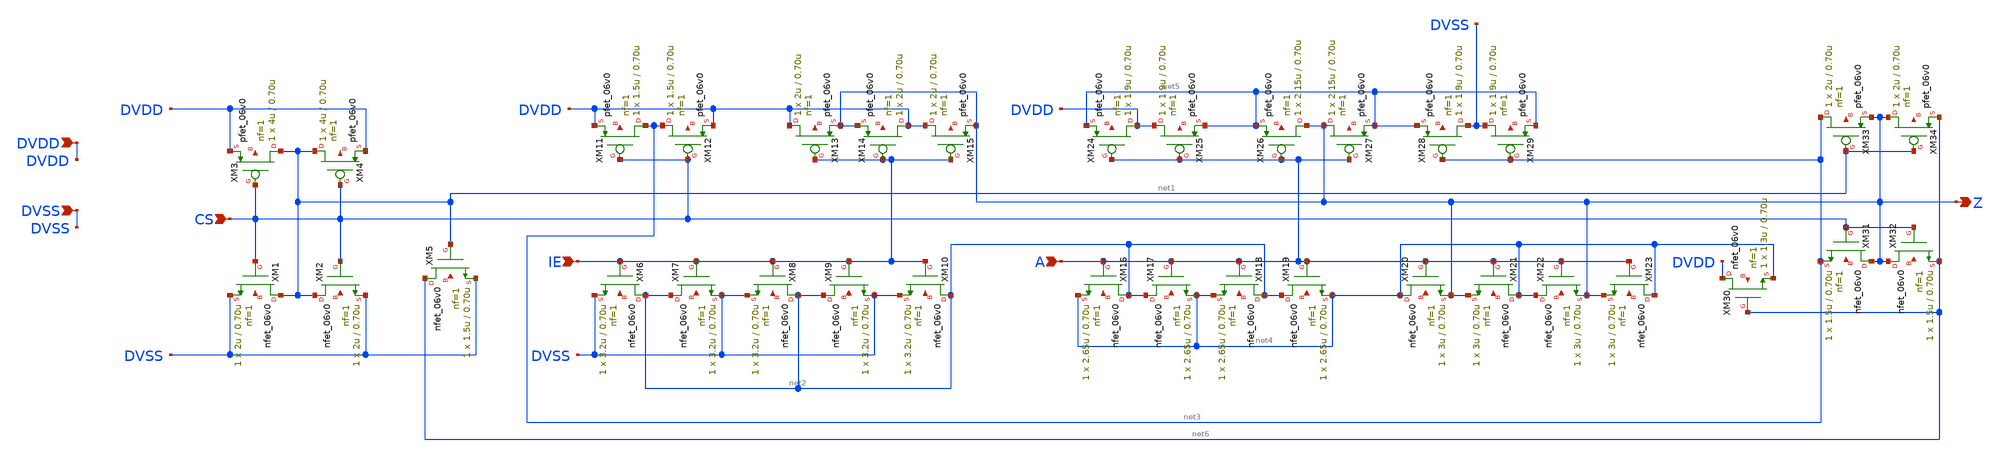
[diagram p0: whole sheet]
** sch_path: gf180mcu_fd_io__bi_24t/comp018green_in_cms_smt.sch
**.subckt comp018green_in_cms_smt CS IE Z A DVDD DVSS
*.ipin CS
*.ipin IE
*.opin Z
*.ipin A
*.ipin DVDD
*.ipin DVSS
XM1 net1 CS DVSS net7 nfet_06v0 L=0.70u W=2u nf=1 ad='int((nf+1)/2) * W/nf * 0.18u' as='int((nf+2)/2) * W/nf * 0.18u'
+ pd='2*int((nf+1)/2) * (W/nf + 0.18u)' ps='2*int((nf+2)/2) * (W/nf + 0.18u)' nrd='0.18u / W' nrs='0.18u / W'
+ sa=0 sb=0 sd=0 m=1
XM2 net1 CS DVSS net8 nfet_06v0 L=0.70u W=2u nf=1 ad='int((nf+1)/2) * W/nf * 0.18u' as='int((nf+2)/2) * W/nf * 0.18u'
+ pd='2*int((nf+1)/2) * (W/nf + 0.18u)' ps='2*int((nf+2)/2) * (W/nf + 0.18u)' nrd='0.18u / W' nrs='0.18u / W'
+ sa=0 sb=0 sd=0 m=1
XM3 net1 CS DVDD net9 pfet_06v0 L=0.70u W=4u nf=1 ad='int((nf+1)/2) * W/nf * 0.18u' as='int((nf+2)/2) * W/nf * 0.18u'
+ pd='2*int((nf+1)/2) * (W/nf + 0.18u)' ps='2*int((nf+2)/2) * (W/nf + 0.18u)' nrd='0.18u / W' nrs='0.18u / W'
+ sa=0 sb=0 sd=0 m=1
XM4 net1 CS DVDD net10 pfet_06v0 L=0.70u W=4u nf=1 ad='int((nf+1)/2) * W/nf * 0.18u' as='int((nf+2)/2) * W/nf * 0.18u'
+ pd='2*int((nf+1)/2) * (W/nf + 0.18u)' ps='2*int((nf+2)/2) * (W/nf + 0.18u)' nrd='0.18u / W' nrs='0.18u / W'
+ sa=0 sb=0 sd=0 m=1
XM5 net6 net1 DVSS net11 nfet_06v0 L=0.70u W=1.5u nf=1 ad='int((nf+1)/2) * W/nf * 0.18u' as='int((nf+2)/2) * W/nf * 0.18u'
+ pd='2*int((nf+1)/2) * (W/nf + 0.18u)' ps='2*int((nf+2)/2) * (W/nf + 0.18u)' nrd='0.18u / W' nrs='0.18u / W'
+ sa=0 sb=0 sd=0 m=1
XM6 net2 IE DVSS net12 nfet_06v0 L=0.70u W=3.2u nf=1 ad='int((nf+1)/2) * W/nf * 0.18u' as='int((nf+2)/2) * W/nf * 0.18u'
+ pd='2*int((nf+1)/2) * (W/nf + 0.18u)' ps='2*int((nf+2)/2) * (W/nf + 0.18u)' nrd='0.18u / W' nrs='0.18u / W'
+ sa=0 sb=0 sd=0 m=1
XM7 net2 IE DVSS net13 nfet_06v0 L=0.70u W=3.2u nf=1 ad='int((nf+1)/2) * W/nf * 0.18u' as='int((nf+2)/2) * W/nf * 0.18u'
+ pd='2*int((nf+1)/2) * (W/nf + 0.18u)' ps='2*int((nf+2)/2) * (W/nf + 0.18u)' nrd='0.18u / W' nrs='0.18u / W'
+ sa=0 sb=0 sd=0 m=1
XM8 net2 IE DVSS net14 nfet_06v0 L=0.70u W=3.2u nf=1 ad='int((nf+1)/2) * W/nf * 0.18u' as='int((nf+2)/2) * W/nf * 0.18u'
+ pd='2*int((nf+1)/2) * (W/nf + 0.18u)' ps='2*int((nf+2)/2) * (W/nf + 0.18u)' nrd='0.18u / W' nrs='0.18u / W'
+ sa=0 sb=0 sd=0 m=1
XM9 net2 IE DVSS net15 nfet_06v0 L=0.70u W=3.2u nf=1 ad='int((nf+1)/2) * W/nf * 0.18u' as='int((nf+2)/2) * W/nf * 0.18u'
+ pd='2*int((nf+1)/2) * (W/nf + 0.18u)' ps='2*int((nf+2)/2) * (W/nf + 0.18u)' nrd='0.18u / W' nrs='0.18u / W'
+ sa=0 sb=0 sd=0 m=1
XM10 net2 IE DVSS net16 nfet_06v0 L=0.70u W=3.2u nf=1 ad='int((nf+1)/2) * W/nf * 0.18u' as='int((nf+2)/2) * W/nf * 0.18u'
+ pd='2*int((nf+1)/2) * (W/nf + 0.18u)' ps='2*int((nf+2)/2) * (W/nf + 0.18u)' nrd='0.18u / W' nrs='0.18u / W'
+ sa=0 sb=0 sd=0 m=1
XM11 net3 CS DVDD net17 pfet_06v0 L=0.70u W=1.5u nf=1 ad='int((nf+1)/2) * W/nf * 0.18u' as='int((nf+2)/2) * W/nf * 0.18u'
+ pd='2*int((nf+1)/2) * (W/nf + 0.18u)' ps='2*int((nf+2)/2) * (W/nf + 0.18u)' nrd='0.18u / W' nrs='0.18u / W'
+ sa=0 sb=0 sd=0 m=1
XM12 net3 CS DVDD net18 pfet_06v0 L=0.70u W=1.5u nf=1 ad='int((nf+1)/2) * W/nf * 0.18u' as='int((nf+2)/2) * W/nf * 0.18u'
+ pd='2*int((nf+1)/2) * (W/nf + 0.18u)' ps='2*int((nf+2)/2) * (W/nf + 0.18u)' nrd='0.18u / W' nrs='0.18u / W'
+ sa=0 sb=0 sd=0 m=1
XM13 DVDD IE Z net19 pfet_06v0 L=0.70u W=2u nf=1 ad='int((nf+1)/2) * W/nf * 0.18u' as='int((nf+2)/2) * W/nf * 0.18u'
+ pd='2*int((nf+1)/2) * (W/nf + 0.18u)' ps='2*int((nf+2)/2) * (W/nf + 0.18u)' nrd='0.18u / W' nrs='0.18u / W'
+ sa=0 sb=0 sd=0 m=1
XM14 DVDD IE Z net20 pfet_06v0 L=0.70u W=2u nf=1 ad='int((nf+1)/2) * W/nf * 0.18u' as='int((nf+2)/2) * W/nf * 0.18u'
+ pd='2*int((nf+1)/2) * (W/nf + 0.18u)' ps='2*int((nf+2)/2) * (W/nf + 0.18u)' nrd='0.18u / W' nrs='0.18u / W'
+ sa=0 sb=0 sd=0 m=1
XM15 DVDD IE Z net21 pfet_06v0 L=0.70u W=2u nf=1 ad='int((nf+1)/2) * W/nf * 0.18u' as='int((nf+2)/2) * W/nf * 0.18u'
+ pd='2*int((nf+1)/2) * (W/nf + 0.18u)' ps='2*int((nf+2)/2) * (W/nf + 0.18u)' nrd='0.18u / W' nrs='0.18u / W'
+ sa=0 sb=0 sd=0 m=1
XM16 net2 A net4 net22 nfet_06v0 L=0.70u W=2.65u nf=1 ad='int((nf+1)/2) * W/nf * 0.18u' as='int((nf+2)/2) * W/nf * 0.18u'
+ pd='2*int((nf+1)/2) * (W/nf + 0.18u)' ps='2*int((nf+2)/2) * (W/nf + 0.18u)' nrd='0.18u / W' nrs='0.18u / W'
+ sa=0 sb=0 sd=0 m=1
XM17 net2 A net4 net23 nfet_06v0 L=0.70u W=2.65u nf=1 ad='int((nf+1)/2) * W/nf * 0.18u' as='int((nf+2)/2) * W/nf * 0.18u'
+ pd='2*int((nf+1)/2) * (W/nf + 0.18u)' ps='2*int((nf+2)/2) * (W/nf + 0.18u)' nrd='0.18u / W' nrs='0.18u / W'
+ sa=0 sb=0 sd=0 m=1
XM18 net2 A net4 net24 nfet_06v0 L=0.70u W=2.65u nf=1 ad='int((nf+1)/2) * W/nf * 0.18u' as='int((nf+2)/2) * W/nf * 0.18u'
+ pd='2*int((nf+1)/2) * (W/nf + 0.18u)' ps='2*int((nf+2)/2) * (W/nf + 0.18u)' nrd='0.18u / W' nrs='0.18u / W'
+ sa=0 sb=0 sd=0 m=1
XM19 net2 A net4 net25 nfet_06v0 L=0.70u W=2.65u nf=1 ad='int((nf+1)/2) * W/nf * 0.18u' as='int((nf+2)/2) * W/nf * 0.18u'
+ pd='2*int((nf+1)/2) * (W/nf + 0.18u)' ps='2*int((nf+2)/2) * (W/nf + 0.18u)' nrd='0.18u / W' nrs='0.18u / W'
+ sa=0 sb=0 sd=0 m=1
XM20 net4 A Z net26 nfet_06v0 L=0.70u W=3u nf=1 ad='int((nf+1)/2) * W/nf * 0.18u' as='int((nf+2)/2) * W/nf * 0.18u'
+ pd='2*int((nf+1)/2) * (W/nf + 0.18u)' ps='2*int((nf+2)/2) * (W/nf + 0.18u)' nrd='0.18u / W' nrs='0.18u / W'
+ sa=0 sb=0 sd=0 m=1
XM21 net4 A Z net27 nfet_06v0 L=0.70u W=3u nf=1 ad='int((nf+1)/2) * W/nf * 0.18u' as='int((nf+2)/2) * W/nf * 0.18u'
+ pd='2*int((nf+1)/2) * (W/nf + 0.18u)' ps='2*int((nf+2)/2) * (W/nf + 0.18u)' nrd='0.18u / W' nrs='0.18u / W'
+ sa=0 sb=0 sd=0 m=1
XM22 net4 A Z net28 nfet_06v0 L=0.70u W=3u nf=1 ad='int((nf+1)/2) * W/nf * 0.18u' as='int((nf+2)/2) * W/nf * 0.18u'
+ pd='2*int((nf+1)/2) * (W/nf + 0.18u)' ps='2*int((nf+2)/2) * (W/nf + 0.18u)' nrd='0.18u / W' nrs='0.18u / W'
+ sa=0 sb=0 sd=0 m=1
XM23 net4 A Z net29 nfet_06v0 L=0.70u W=3u nf=1 ad='int((nf+1)/2) * W/nf * 0.18u' as='int((nf+2)/2) * W/nf * 0.18u'
+ pd='2*int((nf+1)/2) * (W/nf + 0.18u)' ps='2*int((nf+2)/2) * (W/nf + 0.18u)' nrd='0.18u / W' nrs='0.18u / W'
+ sa=0 sb=0 sd=0 m=1
XM24 DVDD A net5 net30 pfet_06v0 L=0.70u W=1.9u nf=1 ad='int((nf+1)/2) * W/nf * 0.18u' as='int((nf+2)/2) * W/nf * 0.18u'
+ pd='2*int((nf+1)/2) * (W/nf + 0.18u)' ps='2*int((nf+2)/2) * (W/nf + 0.18u)' nrd='0.18u / W' nrs='0.18u / W'
+ sa=0 sb=0 sd=0 m=1
XM25 DVDD A net5 net31 pfet_06v0 L=0.70u W=1.9u nf=1 ad='int((nf+1)/2) * W/nf * 0.18u' as='int((nf+2)/2) * W/nf * 0.18u'
+ pd='2*int((nf+1)/2) * (W/nf + 0.18u)' ps='2*int((nf+2)/2) * (W/nf + 0.18u)' nrd='0.18u / W' nrs='0.18u / W'
+ sa=0 sb=0 sd=0 m=1
XM26 Z A net5 net32 pfet_06v0 L=0.70u W=2.15u nf=1 ad='int((nf+1)/2) * W/nf * 0.18u' as='int((nf+2)/2) * W/nf * 0.18u'
+ pd='2*int((nf+1)/2) * (W/nf + 0.18u)' ps='2*int((nf+2)/2) * (W/nf + 0.18u)' nrd='0.18u / W' nrs='0.18u / W'
+ sa=0 sb=0 sd=0 m=1
XM27 Z A net5 net33 pfet_06v0 L=0.70u W=2.15u nf=1 ad='int((nf+1)/2) * W/nf * 0.18u' as='int((nf+2)/2) * W/nf * 0.18u'
+ pd='2*int((nf+1)/2) * (W/nf + 0.18u)' ps='2*int((nf+2)/2) * (W/nf + 0.18u)' nrd='0.18u / W' nrs='0.18u / W'
+ sa=0 sb=0 sd=0 m=1
XM28 DVSS net3 net5 net34 pfet_06v0 L=0.70u W=1.9u nf=1 ad='int((nf+1)/2) * W/nf * 0.18u' as='int((nf+2)/2) * W/nf * 0.18u'
+ pd='2*int((nf+1)/2) * (W/nf + 0.18u)' ps='2*int((nf+2)/2) * (W/nf + 0.18u)' nrd='0.18u / W' nrs='0.18u / W'
+ sa=0 sb=0 sd=0 m=1
XM29 DVSS net3 net5 net35 pfet_06v0 L=0.70u W=1.9u nf=1 ad='int((nf+1)/2) * W/nf * 0.18u' as='int((nf+2)/2) * W/nf * 0.18u'
+ pd='2*int((nf+1)/2) * (W/nf + 0.18u)' ps='2*int((nf+2)/2) * (W/nf + 0.18u)' nrd='0.18u / W' nrs='0.18u / W'
+ sa=0 sb=0 sd=0 m=1
XM30 DVDD net6 net4 net36 nfet_06v0 L=0.70u W=1.3u nf=1 ad='int((nf+1)/2) * W/nf * 0.18u' as='int((nf+2)/2) * W/nf * 0.18u'
+ pd='2*int((nf+1)/2) * (W/nf + 0.18u)' ps='2*int((nf+2)/2) * (W/nf + 0.18u)' nrd='0.18u / W' nrs='0.18u / W'
+ sa=0 sb=0 sd=0 m=1
XM31 Z CS net3 net37 nfet_06v0 L=0.70u W=1.5u nf=1 ad='int((nf+1)/2) * W/nf * 0.18u' as='int((nf+2)/2) * W/nf * 0.18u'
+ pd='2*int((nf+1)/2) * (W/nf + 0.18u)' ps='2*int((nf+2)/2) * (W/nf + 0.18u)' nrd='0.18u / W' nrs='0.18u / W'
+ sa=0 sb=0 sd=0 m=1
XM32 Z CS net6 net38 nfet_06v0 L=0.70u W=1.5u nf=1 ad='int((nf+1)/2) * W/nf * 0.18u' as='int((nf+2)/2) * W/nf * 0.18u'
+ pd='2*int((nf+1)/2) * (W/nf + 0.18u)' ps='2*int((nf+2)/2) * (W/nf + 0.18u)' nrd='0.18u / W' nrs='0.18u / W'
+ sa=0 sb=0 sd=0 m=1
XM33 net3 net1 Z net39 pfet_06v0 L=0.70u W=2u nf=1 ad='int((nf+1)/2) * W/nf * 0.18u' as='int((nf+2)/2) * W/nf * 0.18u'
+ pd='2*int((nf+1)/2) * (W/nf + 0.18u)' ps='2*int((nf+2)/2) * (W/nf + 0.18u)' nrd='0.18u / W' nrs='0.18u / W'
+ sa=0 sb=0 sd=0 m=1
XM34 Z net1 net6 net40 pfet_06v0 L=0.70u W=2u nf=1 ad='int((nf+1)/2) * W/nf * 0.18u' as='int((nf+2)/2) * W/nf * 0.18u'
+ pd='2*int((nf+1)/2) * (W/nf + 0.18u)' ps='2*int((nf+2)/2) * (W/nf + 0.18u)' nrd='0.18u / W' nrs='0.18u / W'
+ sa=0 sb=0 sd=0 m=1
**.ends
.end
